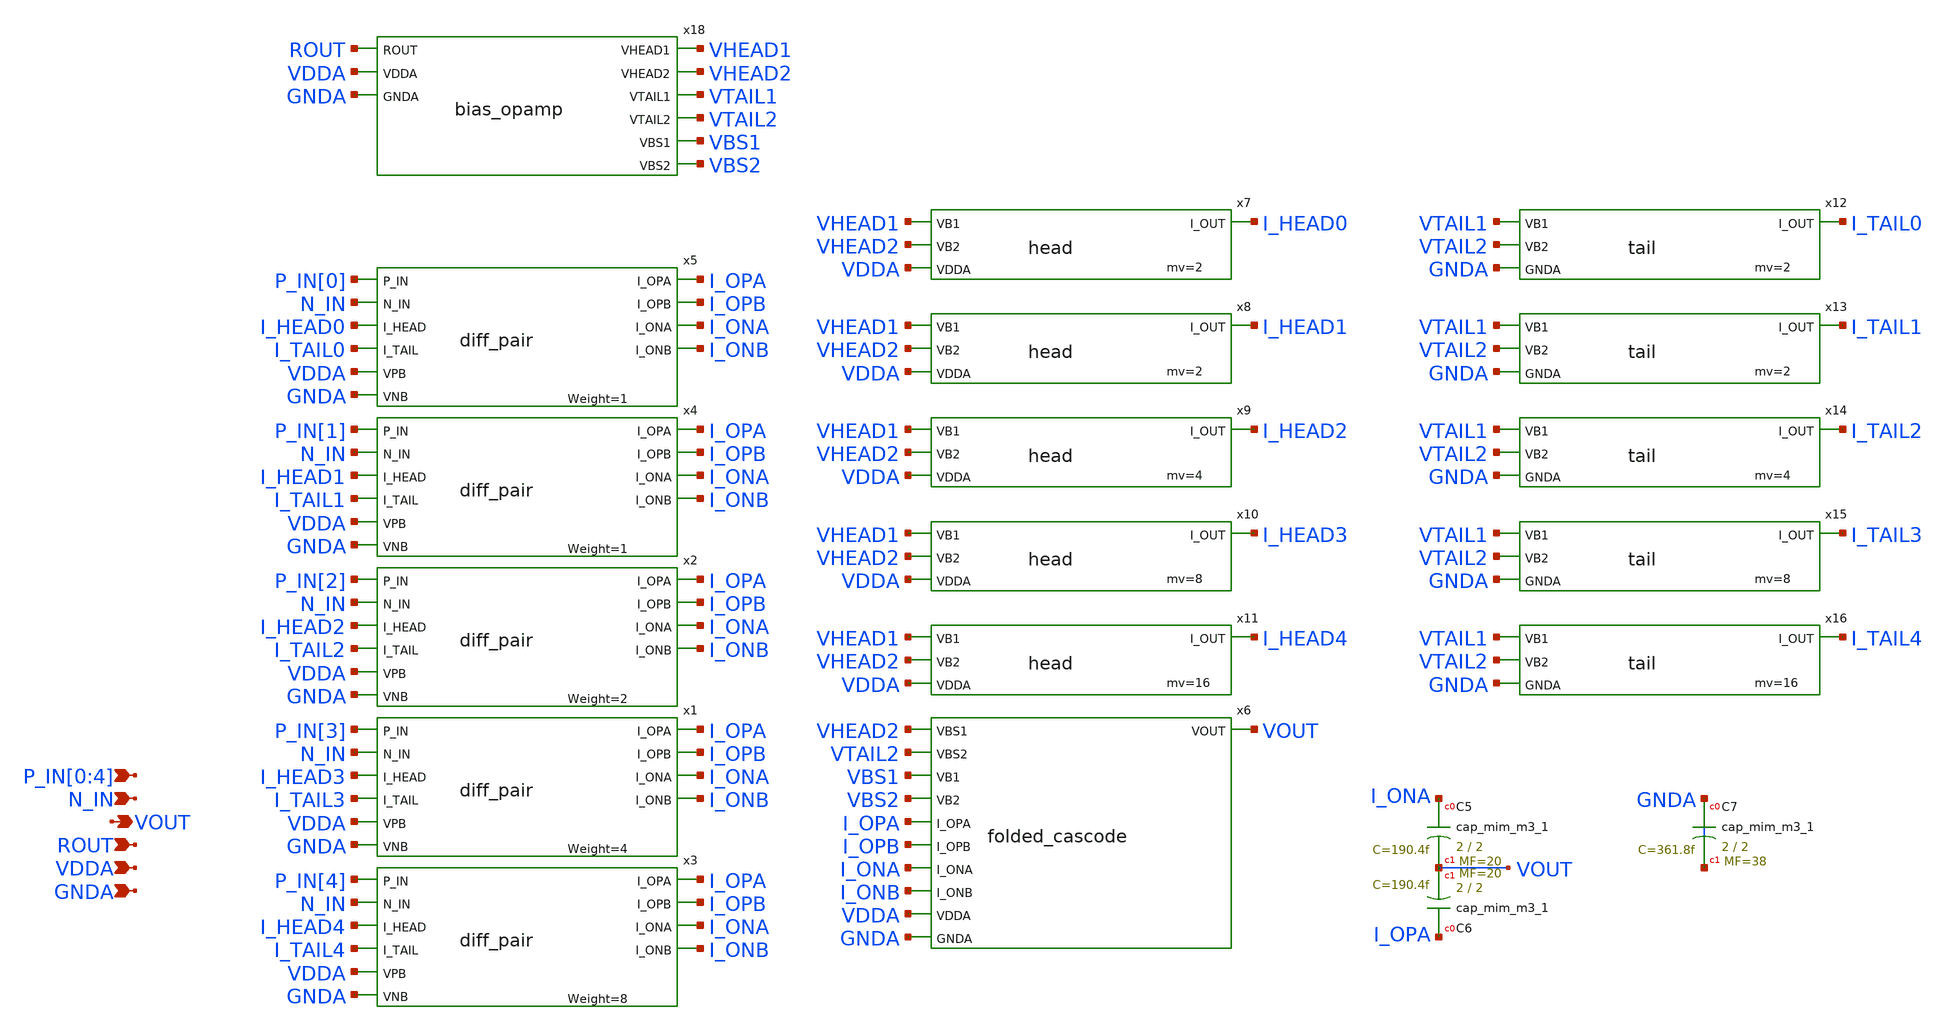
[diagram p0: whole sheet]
** sch_path: xschem/op_amp.sch
**.subckt op_amp P_IN[0],P_IN[1],P_IN[2],P_IN[3],P_IN[4] ROUT VOUT VDDA GNDA N_IN
*.ipin P_IN[0],P_IN[1],P_IN[2],P_IN[3],P_IN[4]
*.ipin ROUT
*.opin VOUT
*.ipin VDDA
*.ipin GNDA
*.ipin N_IN
x7 VHEAD1 VHEAD2 I_HEAD0 VDDA head mv=2
x8 VHEAD1 VHEAD2 I_HEAD1 VDDA head mv=2
x9 VHEAD1 VHEAD2 I_HEAD2 VDDA head mv=4
x10 VHEAD1 VHEAD2 I_HEAD3 VDDA head mv=8
x11 VHEAD1 VHEAD2 I_HEAD4 VDDA head mv=16
x12 VTAIL1 VTAIL2 I_TAIL0 GNDA tail mv=2
x13 VTAIL1 VTAIL2 I_TAIL1 GNDA tail mv=2
x14 VTAIL1 VTAIL2 I_TAIL2 GNDA tail mv=4
x15 VTAIL1 VTAIL2 I_TAIL3 GNDA tail mv=8
x16 VTAIL1 VTAIL2 I_TAIL4 GNDA tail mv=16
x6 VHEAD2 VTAIL2 VBS1 VBS2 I_OPA I_OPB I_ONA I_ONB VOUT VDDA GNDA folded_cascode
x4 P_IN[1] N_IN I_OPA I_OPB I_ONA I_ONB I_HEAD1 I_TAIL1 VDDA GNDA diff_pair
x5 P_IN[0] N_IN I_OPA I_OPB I_ONA I_ONB I_HEAD0 I_TAIL0 VDDA GNDA diff_pair
x18 ROUT VHEAD1 VHEAD2 VTAIL1 VTAIL2 VBS1 VBS2 VDDA GNDA bias_opamp
x1 P_IN[3] N_IN I_OPA I_OPB I_ONA I_ONB I_HEAD3 I_TAIL3 VDDA GNDA diff_pair
x2 P_IN[2] N_IN I_OPA I_OPB I_ONA I_ONB I_HEAD2 I_TAIL2 VDDA GNDA diff_pair
x3 P_IN[4] N_IN I_OPA I_OPB I_ONA I_ONB I_HEAD4 I_TAIL4 VDDA GNDA diff_pair
XC5 I_ONA VOUT sky130_fd_pr__cap_mim_m3_1 W=2 L=2 MF=20 m=20
XC6 I_OPA VOUT sky130_fd_pr__cap_mim_m3_1 W=2 L=2 MF=20 m=20
XC7 GNDA GNDA sky130_fd_pr__cap_mim_m3_1 W=2 L=2 MF=38 m=38
**.ends

* expanding   symbol:  head.sym # of pins=4
** sym_path: xschem/head.sym
** sch_path: xschem/head.sch
.subckt head VB1 VB2 I_OUT VDDA  mv=1
*.opin I_OUT
*.ipin VB1
*.ipin VB2
*.ipin VDDA
XM5 n1 VB1 VDDA VDDA sky130_fd_pr__pfet_g5v0d10v5 L=1 W=1.8 nf=1 ad='int((nf+1)/2) * W/nf * 0.29' as='int((nf+2)/2) * W/nf * 0.29'
+ pd='2*int((nf+1)/2) * (W/nf + 0.29)' ps='2*int((nf+2)/2) * (W/nf + 0.29)' nrd='0.29 / W' nrs='0.29 / W'
+ sa=0 sb=0 sd=0 mult=mv m=mv
XM1 net1 VB2 n1 VDDA sky130_fd_pr__pfet_g5v0d10v5 L=1 W=1.8 nf=1 ad='int((nf+1)/2) * W/nf * 0.29' as='int((nf+2)/2) * W/nf * 0.29'
+ pd='2*int((nf+1)/2) * (W/nf + 0.29)' ps='2*int((nf+2)/2) * (W/nf + 0.29)' nrd='0.29 / W' nrs='0.29 / W'
+ sa=0 sb=0 sd=0 mult=mv m=mv
Vmeas net1 I_OUT 0
.save i(vmeas)
.ends


* expanding   symbol:  tail.sym # of pins=4
** sym_path: xschem/tail.sym
** sch_path: xschem/tail.sch
.subckt tail VB1 VB2 I_OUT GNDA  mv=1
*.opin I_OUT
*.ipin VB1
*.ipin VB2
*.ipin GNDA
XM1 net1 VB2 n1 GNDA sky130_fd_pr__nfet_g5v0d10v5 L=1 W=0.6 nf=1 ad='int((nf+1)/2) * W/nf * 0.29' as='int((nf+2)/2) * W/nf * 0.29'
+ pd='2*int((nf+1)/2) * (W/nf + 0.29)' ps='2*int((nf+2)/2) * (W/nf + 0.29)' nrd='0.29 / W' nrs='0.29 / W'
+ sa=0 sb=0 sd=0 mult=mv m=mv
XM2 n1 VB1 GNDA GNDA sky130_fd_pr__nfet_g5v0d10v5 L=1 W=0.6 nf=1 ad='int((nf+1)/2) * W/nf * 0.29' as='int((nf+2)/2) * W/nf * 0.29'
+ pd='2*int((nf+1)/2) * (W/nf + 0.29)' ps='2*int((nf+2)/2) * (W/nf + 0.29)' nrd='0.29 / W' nrs='0.29 / W'
+ sa=0 sb=0 sd=0 mult=mv m=mv
Vmeas I_OUT net1 0
.save i(vmeas)
.ends


* expanding   symbol:  folded_cascode.sym # of pins=11
** sym_path: xschem/folded_cascode.sym
** sch_path: xschem/folded_cascode.sch
.subckt folded_cascode VBS1 VBS2 VB1 VB2 I_OPA I_OPB I_ONA I_ONB VOUT VDDA GNDA
*.ipin I_OPA
*.ipin I_OPB
*.ipin I_ONA
*.ipin I_ONB
*.opin VOUT
*.ipin VBS1
*.ipin VBS2
*.ipin VB1
*.ipin VB2
*.ipin VDDA
*.ipin GNDA
.param wp_sum=4.8 wn_sum=1.6 l_sum=1 m_sum=2 wp_fcm=4.8 wn_fcm=1.6 m_fcm=2

XM1 I_ONB VGP net1 net1 sky130_fd_pr__pfet_g5v0d10v5 L=1 W=4.8 nf=1 ad='int((nf+1)/2) * W/nf * 0.29'
+ as='int((nf+2)/2) * W/nf * 0.29' pd='2*int((nf+1)/2) * (W/nf + 0.29)' ps='2*int((nf+2)/2) * (W/nf + 0.29)'
+ nrd='0.29 / W' nrs='0.29 / W' sa=0 sb=0 sd=0 mult=2 m=2
XM8 VGP VB2 VGN GNDA sky130_fd_pr__nfet_g5v0d10v5 L=1 W=1.6 nf=1 ad='int((nf+1)/2) * W/nf * 0.29' as='int((nf+2)/2) * W/nf * 0.29'
+ pd='2*int((nf+1)/2) * (W/nf + 0.29)' ps='2*int((nf+2)/2) * (W/nf + 0.29)' nrd='0.29 / W' nrs='0.29 / W'
+ sa=0 sb=0 sd=0 mult=2 m=2
XM13 GNDA GNDA GNDA GNDA sky130_fd_pr__nfet_g5v0d10v5 L=1 W=1.6 nf=1 ad='int((nf+1)/2) * W/nf * 0.29'
+ as='int((nf+2)/2) * W/nf * 0.29' pd='2*int((nf+1)/2) * (W/nf + 0.29)' ps='2*int((nf+2)/2) * (W/nf + 0.29)'
+ nrd='0.29 / W' nrs='0.29 / W' sa=0 sb=0 sd=0 mult=4 m=4
XM2 I_ONA VGP net2 net2 sky130_fd_pr__pfet_g5v0d10v5 L=1 W=4.8 nf=1 ad='int((nf+1)/2) * W/nf * 0.29'
+ as='int((nf+2)/2) * W/nf * 0.29' pd='2*int((nf+1)/2) * (W/nf + 0.29)' ps='2*int((nf+2)/2) * (W/nf + 0.29)'
+ nrd='0.29 / W' nrs='0.29 / W' sa=0 sb=0 sd=0 mult=2 m=2
XM3 net7 VBS1 I_ONB net1 sky130_fd_pr__pfet_g5v0d10v5 L=1 W=4.8 nf=1 ad='int((nf+1)/2) * W/nf * 0.29'
+ as='int((nf+2)/2) * W/nf * 0.29' pd='2*int((nf+1)/2) * (W/nf + 0.29)' ps='2*int((nf+2)/2) * (W/nf + 0.29)'
+ nrd='0.29 / W' nrs='0.29 / W' sa=0 sb=0 sd=0 mult=2 m=2
XM4 net8 VBS1 I_ONA net2 sky130_fd_pr__pfet_g5v0d10v5 L=1 W=4.8 nf=1 ad='int((nf+1)/2) * W/nf * 0.29'
+ as='int((nf+2)/2) * W/nf * 0.29' pd='2*int((nf+1)/2) * (W/nf + 0.29)' ps='2*int((nf+2)/2) * (W/nf + 0.29)'
+ nrd='0.29 / W' nrs='0.29 / W' sa=0 sb=0 sd=0 mult=2 m=2
XM5 VGN VB1 VGP VDDA sky130_fd_pr__pfet_g5v0d10v5 L=1 W=4.8 nf=1 ad='int((nf+1)/2) * W/nf * 0.29' as='int((nf+2)/2) * W/nf * 0.29'
+ pd='2*int((nf+1)/2) * (W/nf + 0.29)' ps='2*int((nf+2)/2) * (W/nf + 0.29)' nrd='0.29 / W' nrs='0.29 / W'
+ sa=0 sb=0 sd=0 mult=2 m=2
XM6 B VB1 A VDDA sky130_fd_pr__pfet_g5v0d10v5 L=1 W=4.8 nf=1 ad='int((nf+1)/2) * W/nf * 0.29' as='int((nf+2)/2) * W/nf * 0.29'
+ pd='2*int((nf+1)/2) * (W/nf + 0.29)' ps='2*int((nf+2)/2) * (W/nf + 0.29)' nrd='0.29 / W' nrs='0.29 / W'
+ sa=0 sb=0 sd=0 mult=2 m=2
XM7 A VB2 B GNDA sky130_fd_pr__nfet_g5v0d10v5 L=1 W=1.6 nf=1 ad='int((nf+1)/2) * W/nf * 0.29' as='int((nf+2)/2) * W/nf * 0.29'
+ pd='2*int((nf+1)/2) * (W/nf + 0.29)' ps='2*int((nf+2)/2) * (W/nf + 0.29)' nrd='0.29 / W' nrs='0.29 / W'
+ sa=0 sb=0 sd=0 mult=2 m=2
XM10 net9 VBS2 I_OPB net3 sky130_fd_pr__nfet_g5v0d10v5 L=1 W=1.6 nf=1 ad='int((nf+1)/2) * W/nf * 0.29'
+ as='int((nf+2)/2) * W/nf * 0.29' pd='2*int((nf+1)/2) * (W/nf + 0.29)' ps='2*int((nf+2)/2) * (W/nf + 0.29)'
+ nrd='0.29 / W' nrs='0.29 / W' sa=0 sb=0 sd=0 mult=2 m=2
XM11 net10 VBS2 I_OPA net4 sky130_fd_pr__nfet_g5v0d10v5 L=1 W=1.6 nf=1 ad='int((nf+1)/2) * W/nf * 0.29'
+ as='int((nf+2)/2) * W/nf * 0.29' pd='2*int((nf+1)/2) * (W/nf + 0.29)' ps='2*int((nf+2)/2) * (W/nf + 0.29)'
+ nrd='0.29 / W' nrs='0.29 / W' sa=0 sb=0 sd=0 mult=2 m=2
XM9 I_OPB VGN net3 net3 sky130_fd_pr__nfet_g5v0d10v5 L=1 W=1.6 nf=1 ad='int((nf+1)/2) * W/nf * 0.29'
+ as='int((nf+2)/2) * W/nf * 0.29' pd='2*int((nf+1)/2) * (W/nf + 0.29)' ps='2*int((nf+2)/2) * (W/nf + 0.29)'
+ nrd='0.29 / W' nrs='0.29 / W' sa=0 sb=0 sd=0 mult=6 m=6
XM12 I_OPA VGN net4 net4 sky130_fd_pr__nfet_g5v0d10v5 L=1 W=1.6 nf=1 ad='int((nf+1)/2) * W/nf * 0.29'
+ as='int((nf+2)/2) * W/nf * 0.29' pd='2*int((nf+1)/2) * (W/nf + 0.29)' ps='2*int((nf+2)/2) * (W/nf + 0.29)'
+ nrd='0.29 / W' nrs='0.29 / W' sa=0 sb=0 sd=0 mult=6 m=6
XM14 VOUT B net6 net6 sky130_fd_pr__nfet_g5v0d10v5 L=1 W=2 nf=1 ad='int((nf+1)/2) * W/nf * 0.29' as='int((nf+2)/2) * W/nf * 0.29'
+ pd='2*int((nf+1)/2) * (W/nf + 0.29)' ps='2*int((nf+2)/2) * (W/nf + 0.29)' nrd='0.29 / W' nrs='0.29 / W'
+ sa=0 sb=0 sd=0 mult=2 m=2
XM15 VOUT A net5 net5 sky130_fd_pr__pfet_g5v0d10v5 L=1 W=6 nf=1 ad='int((nf+1)/2) * W/nf * 0.29' as='int((nf+2)/2) * W/nf * 0.29'
+ pd='2*int((nf+1)/2) * (W/nf + 0.29)' ps='2*int((nf+2)/2) * (W/nf + 0.29)' nrd='0.29 / W' nrs='0.29 / W'
+ sa=0 sb=0 sd=0 mult=2 m=2
Vmeas net3 GNDA 0
.save i(vmeas)
Vmeas1 net4 GNDA 0
.save i(vmeas1)
Vmeas2 VGN net9 0
.save i(vmeas2)
Vmeas3 B net10 0
.save i(vmeas3)
Vmeas4 VDDA net1 0
.save i(vmeas4)
Vmeas5 VDDA net2 0
.save i(vmeas5)
Vmeas6 net7 VGP 0
.save i(vmeas6)
Vmeas7 net8 A 0
.save i(vmeas7)
Vmeas8 VDDA net5 0
.save i(vmeas8)
Vmeas9 net6 GNDA 0
.save i(vmeas9)
.ends


* expanding   symbol:  diff_pair.sym # of pins=10
** sym_path: xschem/diff_pair.sym
** sch_path: xschem/diff_pair.sch
.subckt diff_pair P_IN N_IN I_OPA I_OPB I_ONA I_ONB I_HEAD I_TAIL VPB VNB  weight=1
*.opin I_OPA
*.opin I_OPB
*.ipin P_IN
*.ipin N_IN
*.opin I_ONA
*.opin I_ONB
*.ipin I_HEAD
*.ipin I_TAIL
*.ipin VPB
*.ipin VNB
XM1 I_OPA P_IN I_HEAD VPB sky130_fd_pr__pfet_g5v0d10v5 L=l_diff W=wp_diff nf=1 ad='int((nf+1)/2) * W/nf * 0.29'
+ as='int((nf+2)/2) * W/nf * 0.29' pd='2*int((nf+1)/2) * (W/nf + 0.29)' ps='2*int((nf+2)/2) * (W/nf + 0.29)'
+ nrd='0.29 / W' nrs='0.29 / W' sa=0 sb=0 sd=0 mult=2 m=2
XM3 I_ONA P_IN I_TAIL VNB sky130_fd_pr__nfet_g5v0d10v5 L=l_diff W=wn_diff nf=1 ad='int((nf+1)/2) * W/nf * 0.29'
+ as='int((nf+2)/2) * W/nf * 0.29' pd='2*int((nf+1)/2) * (W/nf + 0.29)' ps='2*int((nf+2)/2) * (W/nf + 0.29)'
+ nrd='0.29 / W' nrs='0.29 / W' sa=0 sb=0 sd=0 mult=2 m=2
.param wp_diff=3 wn_diff=1 l_diff=1

XM2 I_OPB N_IN I_HEAD VPB sky130_fd_pr__pfet_g5v0d10v5 L=l_diff W=wp_diff nf=1 ad='int((nf+1)/2) * W/nf * 0.29'
+ as='int((nf+2)/2) * W/nf * 0.29' pd='2*int((nf+1)/2) * (W/nf + 0.29)' ps='2*int((nf+2)/2) * (W/nf + 0.29)'
+ nrd='0.29 / W' nrs='0.29 / W' sa=0 sb=0 sd=0 mult=2 m=2
XM4 I_ONB N_IN I_TAIL VNB sky130_fd_pr__nfet_g5v0d10v5 L=l_diff W=wn_diff nf=1 ad='int((nf+1)/2) * W/nf * 0.29'
+ as='int((nf+2)/2) * W/nf * 0.29' pd='2*int((nf+1)/2) * (W/nf + 0.29)' ps='2*int((nf+2)/2) * (W/nf + 0.29)'
+ nrd='0.29 / W' nrs='0.29 / W' sa=0 sb=0 sd=0 mult=2 m=2
.ends


* expanding   symbol:  bias_opamp.sym # of pins=9
** sym_path: xschem/bias_opamp.sym
** sch_path: xschem/bias_opamp.sch
.subckt bias_opamp ROUT VHEAD1 VHEAD2 VTAIL1 VTAIL2 VBS1 VBS2 VDDA GNDA
*.ipin ROUT
*.opin VHEAD1
*.ipin VDDA
*.ipin GNDA
*.opin VHEAD2
*.opin VTAIL1
*.opin VTAIL2
*.opin VBS1
*.opin VBS2
.param wp_iref=1.8 wn_iref=0.6 miref=20 miref2=8 wp_bias=4.8 wn_bias=1.6 mbias=2 l=1 lref=1 lr=20
XM1 net1 VHEAD1 VDDA VDDA sky130_fd_pr__pfet_g5v0d10v5 L=1 W=1.8 nf=1 ad='int((nf+1)/2) * W/nf * 0.29'
+ as='int((nf+2)/2) * W/nf * 0.29' pd='2*int((nf+1)/2) * (W/nf + 0.29)' ps='2*int((nf+2)/2) * (W/nf + 0.29)'
+ nrd='0.29 / W' nrs='0.29 / W' sa=0 sb=0 sd=0 mult=20 m=20
XM2 VHEAD1 VHEAD2 net1 VDDA sky130_fd_pr__pfet_g5v0d10v5 L=1 W=1.8 nf=1 ad='int((nf+1)/2) * W/nf * 0.29'
+ as='int((nf+2)/2) * W/nf * 0.29' pd='2*int((nf+1)/2) * (W/nf + 0.29)' ps='2*int((nf+2)/2) * (W/nf + 0.29)'
+ nrd='0.29 / W' nrs='0.29 / W' sa=0 sb=0 sd=0 mult=20 m=20
XM7 net6 VHEAD1 VDDA VDDA sky130_fd_pr__pfet_g5v0d10v5 L=1 W=1.8 nf=1 ad='int((nf+1)/2) * W/nf * 0.29'
+ as='int((nf+2)/2) * W/nf * 0.29' pd='2*int((nf+1)/2) * (W/nf + 0.29)' ps='2*int((nf+2)/2) * (W/nf + 0.29)'
+ nrd='0.29 / W' nrs='0.29 / W' sa=0 sb=0 sd=0 mult=20 m=20
XM8 net5 VHEAD2 net6 VDDA sky130_fd_pr__pfet_g5v0d10v5 L=1 W=1.8 nf=1 ad='int((nf+1)/2) * W/nf * 0.29'
+ as='int((nf+2)/2) * W/nf * 0.29' pd='2*int((nf+1)/2) * (W/nf + 0.29)' ps='2*int((nf+2)/2) * (W/nf + 0.29)'
+ nrd='0.29 / W' nrs='0.29 / W' sa=0 sb=0 sd=0 mult=20 m=20
XM3 VHEAD2 net2 VHEAD1 VDDA sky130_fd_pr__pfet_g5v0d10v5 L=20 W=1.8 nf=1 ad='int((nf+1)/2) * W/nf * 0.29'
+ as='int((nf+2)/2) * W/nf * 0.29' pd='2*int((nf+1)/2) * (W/nf + 0.29)' ps='2*int((nf+2)/2) * (W/nf + 0.29)'
+ nrd='0.29 / W' nrs='0.29 / W' sa=0 sb=0 sd=0 mult=2 m=2
XM4 net2 net2 VHEAD2 VDDA sky130_fd_pr__pfet_g5v0d10v5 L=20 W=1.8 nf=1 ad='int((nf+1)/2) * W/nf * 0.29'
+ as='int((nf+2)/2) * W/nf * 0.29' pd='2*int((nf+1)/2) * (W/nf + 0.29)' ps='2*int((nf+2)/2) * (W/nf + 0.29)'
+ nrd='0.29 / W' nrs='0.29 / W' sa=0 sb=0 sd=0 mult=2 m=2
XM5 net3 net9 net2 VDDA sky130_fd_pr__pfet_g5v0d10v5 L=20 W=1.8 nf=1 ad='int((nf+1)/2) * W/nf * 0.29'
+ as='int((nf+2)/2) * W/nf * 0.29' pd='2*int((nf+1)/2) * (W/nf + 0.29)' ps='2*int((nf+2)/2) * (W/nf + 0.29)'
+ nrd='0.29 / W' nrs='0.29 / W' sa=0 sb=0 sd=0 mult=2 m=2
XM6 net9 net9 net3 VDDA sky130_fd_pr__pfet_g5v0d10v5 L=20 W=1.8 nf=1 ad='int((nf+1)/2) * W/nf * 0.29'
+ as='int((nf+2)/2) * W/nf * 0.29' pd='2*int((nf+1)/2) * (W/nf + 0.29)' ps='2*int((nf+2)/2) * (W/nf + 0.29)'
+ nrd='0.29 / W' nrs='0.29 / W' sa=0 sb=0 sd=0 mult=2 m=2
XM13 net7 VHEAD1 VDDA VDDA sky130_fd_pr__pfet_g5v0d10v5 L=1 W=1.8 nf=1 ad='int((nf+1)/2) * W/nf * 0.29'
+ as='int((nf+2)/2) * W/nf * 0.29' pd='2*int((nf+1)/2) * (W/nf + 0.29)' ps='2*int((nf+2)/2) * (W/nf + 0.29)'
+ nrd='0.29 / W' nrs='0.29 / W' sa=0 sb=0 sd=0 mult=8 m=8
XM14 VBS2 VHEAD2 net7 VDDA sky130_fd_pr__pfet_g5v0d10v5 L=1 W=1.8 nf=1 ad='int((nf+1)/2) * W/nf * 0.29'
+ as='int((nf+2)/2) * W/nf * 0.29' pd='2*int((nf+1)/2) * (W/nf + 0.29)' ps='2*int((nf+2)/2) * (W/nf + 0.29)'
+ nrd='0.29 / W' nrs='0.29 / W' sa=0 sb=0 sd=0 mult=8 m=8
XM17 PVB PVB VDDA VDDA sky130_fd_pr__pfet_g5v0d10v5 L=1 W=4.8 nf=1 ad='int((nf+1)/2) * W/nf * 0.29' as='int((nf+2)/2) * W/nf * 0.29'
+ pd='2*int((nf+1)/2) * (W/nf + 0.29)' ps='2*int((nf+2)/2) * (W/nf + 0.29)' nrd='0.29 / W' nrs='0.29 / W'
+ sa=0 sb=0 sd=0 mult=2 m=2
XM18 VBS1 VBS1 PVB VDDA sky130_fd_pr__pfet_g5v0d10v5 L=1 W=4.8 nf=1 ad='int((nf+1)/2) * W/nf * 0.29'
+ as='int((nf+2)/2) * W/nf * 0.29' pd='2*int((nf+1)/2) * (W/nf + 0.29)' ps='2*int((nf+2)/2) * (W/nf + 0.29)'
+ nrd='0.29 / W' nrs='0.29 / W' sa=0 sb=0 sd=0 mult=2 m=2
XM11 net4 VTAIL1 net10 net10 sky130_fd_pr__nfet_g5v0d10v5 L=1 W=0.6 nf=1 ad='int((nf+1)/2) * W/nf * 0.29'
+ as='int((nf+2)/2) * W/nf * 0.29' pd='2*int((nf+1)/2) * (W/nf + 0.29)' ps='2*int((nf+2)/2) * (W/nf + 0.29)'
+ nrd='0.29 / W' nrs='0.29 / W' sa=0 sb=0 sd=0 mult=20 m=20
XM12 VTAIL1 VTAIL2 net4 net10 sky130_fd_pr__nfet_g5v0d10v5 L=1 W=0.6 nf=1 ad='int((nf+1)/2) * W/nf * 0.29'
+ as='int((nf+2)/2) * W/nf * 0.29' pd='2*int((nf+1)/2) * (W/nf + 0.29)' ps='2*int((nf+2)/2) * (W/nf + 0.29)'
+ nrd='0.29 / W' nrs='0.29 / W' sa=0 sb=0 sd=0 mult=20 m=20
XM9 net5 net5 VTAIL2 net10 sky130_fd_pr__nfet_g5v0d10v5 L=20 W=0.6 nf=1 ad='int((nf+1)/2) * W/nf * 0.29'
+ as='int((nf+2)/2) * W/nf * 0.29' pd='2*int((nf+1)/2) * (W/nf + 0.29)' ps='2*int((nf+2)/2) * (W/nf + 0.29)'
+ nrd='0.29 / W' nrs='0.29 / W' sa=0 sb=0 sd=0 mult=2 m=2
XM10 VTAIL2 net5 VTAIL1 net10 sky130_fd_pr__nfet_g5v0d10v5 L=20 W=0.6 nf=1 ad='int((nf+1)/2) * W/nf * 0.29'
+ as='int((nf+2)/2) * W/nf * 0.29' pd='2*int((nf+1)/2) * (W/nf + 0.29)' ps='2*int((nf+2)/2) * (W/nf + 0.29)'
+ nrd='0.29 / W' nrs='0.29 / W' sa=0 sb=0 sd=0 mult=2 m=2
XM22 GNDA GNDA GNDA GNDA sky130_fd_pr__nfet_g5v0d10v5 L=1 W=0.6 nf=1 ad='int((nf+1)/2) * W/nf * 0.29'
+ as='int((nf+2)/2) * W/nf * 0.29' pd='2*int((nf+1)/2) * (W/nf + 0.29)' ps='2*int((nf+2)/2) * (W/nf + 0.29)'
+ nrd='0.29 / W' nrs='0.29 / W' sa=0 sb=0 sd=0 mult=6 m=6
XM19 net8 VTAIL1 net11 net11 sky130_fd_pr__nfet_g5v0d10v5 L=1 W=0.6 nf=1 ad='int((nf+1)/2) * W/nf * 0.29'
+ as='int((nf+2)/2) * W/nf * 0.29' pd='2*int((nf+1)/2) * (W/nf + 0.29)' ps='2*int((nf+2)/2) * (W/nf + 0.29)'
+ nrd='0.29 / W' nrs='0.29 / W' sa=0 sb=0 sd=0 mult=8 m=8
XM20 VBS1 VTAIL2 net8 net11 sky130_fd_pr__nfet_g5v0d10v5 L=1 W=0.6 nf=1 ad='int((nf+1)/2) * W/nf * 0.29'
+ as='int((nf+2)/2) * W/nf * 0.29' pd='2*int((nf+1)/2) * (W/nf + 0.29)' ps='2*int((nf+2)/2) * (W/nf + 0.29)'
+ nrd='0.29 / W' nrs='0.29 / W' sa=0 sb=0 sd=0 mult=8 m=8
XM15 NVB NVB net12 net12 sky130_fd_pr__nfet_g5v0d10v5 L=1 W=1.6 nf=1 ad='int((nf+1)/2) * W/nf * 0.29'
+ as='int((nf+2)/2) * W/nf * 0.29' pd='2*int((nf+1)/2) * (W/nf + 0.29)' ps='2*int((nf+2)/2) * (W/nf + 0.29)'
+ nrd='0.29 / W' nrs='0.29 / W' sa=0 sb=0 sd=0 mult=2 m=2
XM16 VBS2 VBS2 NVB net12 sky130_fd_pr__nfet_g5v0d10v5 L=1 W=1.6 nf=1 ad='int((nf+1)/2) * W/nf * 0.29'
+ as='int((nf+2)/2) * W/nf * 0.29' pd='2*int((nf+1)/2) * (W/nf + 0.29)' ps='2*int((nf+2)/2) * (W/nf + 0.29)'
+ nrd='0.29 / W' nrs='0.29 / W' sa=0 sb=0 sd=0 mult=2 m=2
XM23 GNDA GNDA GNDA GNDA sky130_fd_pr__nfet_g5v0d10v5 L=1 W=0.6 nf=1 ad='int((nf+1)/2) * W/nf * 0.29'
+ as='int((nf+2)/2) * W/nf * 0.29' pd='2*int((nf+1)/2) * (W/nf + 0.29)' ps='2*int((nf+2)/2) * (W/nf + 0.29)'
+ nrd='0.29 / W' nrs='0.29 / W' sa=0 sb=0 sd=0 mult=6 m=6
XM24 VDDA VDDA VDDA VDDA sky130_fd_pr__pfet_g5v0d10v5 L=1 W=1.8 nf=1 ad='int((nf+1)/2) * W/nf * 0.29'
+ as='int((nf+2)/2) * W/nf * 0.29' pd='2*int((nf+1)/2) * (W/nf + 0.29)' ps='2*int((nf+2)/2) * (W/nf + 0.29)'
+ nrd='0.29 / W' nrs='0.29 / W' sa=0 sb=0 sd=0 mult=8 m=8
XM25 VDDA VDDA VDDA VDDA sky130_fd_pr__pfet_g5v0d10v5 L=1 W=1.8 nf=1 ad='int((nf+1)/2) * W/nf * 0.29'
+ as='int((nf+2)/2) * W/nf * 0.29' pd='2*int((nf+1)/2) * (W/nf + 0.29)' ps='2*int((nf+2)/2) * (W/nf + 0.29)'
+ nrd='0.29 / W' nrs='0.29 / W' sa=0 sb=0 sd=0 mult=16 m=16
XM26 VDDA VDDA VDDA VDDA sky130_fd_pr__pfet_g5v0d10v5 L=1 W=1.8 nf=1 ad='int((nf+1)/2) * W/nf * 0.29'
+ as='int((nf+2)/2) * W/nf * 0.29' pd='2*int((nf+1)/2) * (W/nf + 0.29)' ps='2*int((nf+2)/2) * (W/nf + 0.29)'
+ nrd='0.29 / W' nrs='0.29 / W' sa=0 sb=0 sd=0 mult=16 m=16
XM27 GNDA GNDA GNDA GNDA sky130_fd_pr__nfet_g5v0d10v5 L=1 W=0.6 nf=1 ad='int((nf+1)/2) * W/nf * 0.29'
+ as='int((nf+2)/2) * W/nf * 0.29' pd='2*int((nf+1)/2) * (W/nf + 0.29)' ps='2*int((nf+2)/2) * (W/nf + 0.29)'
+ nrd='0.29 / W' nrs='0.29 / W' sa=0 sb=0 sd=0 mult=4 m=4
Vmeas net9 ROUT 0
.save i(vmeas)
Vmeas1 net10 GNDA 0
.save i(vmeas1)
Vmeas2 net12 GNDA 0
.save i(vmeas2)
Vmeas3 net11 GNDA 0
.save i(vmeas3)
.ends

.end
